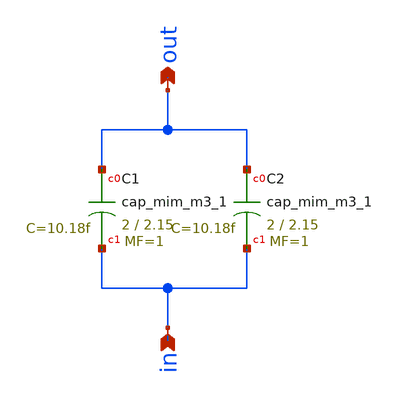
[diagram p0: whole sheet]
** sch_path: xschem/cap2.sch
**.subckt cap2 in out
*.ipin in
*.opin out
XC1 out in sky130_fd_pr__cap_mim_m3_1 W=2 L=2.15 MF=1 m=1
XC2 out in sky130_fd_pr__cap_mim_m3_1 W=2 L=2.15 MF=1 m=1
**.ends
.end
